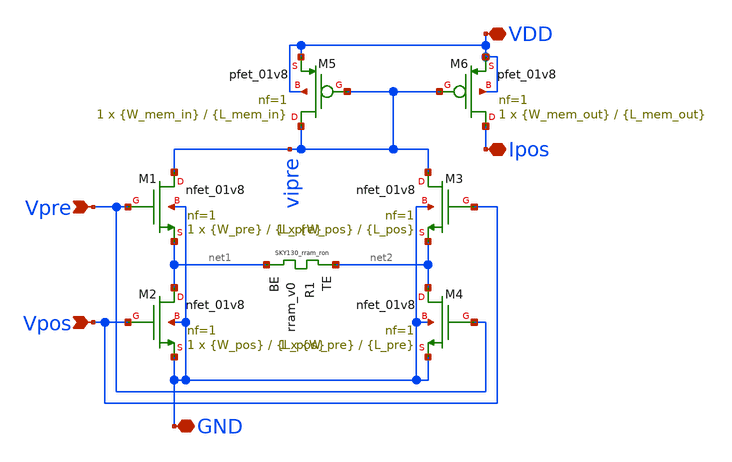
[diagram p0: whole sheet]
** sch_path: SNN/Syn_6T1R.sch
**.subckt Syn_6T1R Vpre Vpos GND Ipos VDD
*.ipin Vpre
*.ipin Vpos
*.iopin GND
*.iopin Ipos
*.iopin VDD
XM1 vipre Vpre net1 GND sky130_fd_pr__nfet_01v8 L={L_pre} W={W_pre} nf=1 ad='int((nf+1)/2) * W/nf * 0.29'
+ as='int((nf+2)/2) * W/nf * 0.29' pd='2*int((nf+1)/2) * (W/nf + 0.29)' ps='2*int((nf+2)/2) * (W/nf + 0.29)'
+ nrd='0.29 / W' nrs='0.29 / W' sa=0 sb=0 sd=0 mult=1 m=1
XR1 net2 net1 rram_v0
XM3 vipre Vpos net2 GND sky130_fd_pr__nfet_01v8 L={L_pos} W={W_pos} nf=1 ad='int((nf+1)/2) * W/nf * 0.29'
+ as='int((nf+2)/2) * W/nf * 0.29' pd='2*int((nf+1)/2) * (W/nf + 0.29)' ps='2*int((nf+2)/2) * (W/nf + 0.29)'
+ nrd='0.29 / W' nrs='0.29 / W' sa=0 sb=0 sd=0 mult=1 m=1
XM6 Ipos vipre VDD VDD sky130_fd_pr__pfet_01v8 L={L_mem_out} W={W_mem_out} nf=1 ad='int((nf+1)/2) * W/nf * 0.29'
+ as='int((nf+2)/2) * W/nf * 0.29' pd='2*int((nf+1)/2) * (W/nf + 0.29)' ps='2*int((nf+2)/2) * (W/nf + 0.29)'
+ nrd='0.29 / W' nrs='0.29 / W' sa=0 sb=0 sd=0 mult=1 m=1
XM5 vipre vipre VDD VDD sky130_fd_pr__pfet_01v8 L={L_mem_in} W={W_mem_in} nf=1 ad='int((nf+1)/2) * W/nf * 0.29'
+ as='int((nf+2)/2) * W/nf * 0.29' pd='2*int((nf+1)/2) * (W/nf + 0.29)' ps='2*int((nf+2)/2) * (W/nf + 0.29)'
+ nrd='0.29 / W' nrs='0.29 / W' sa=0 sb=0 sd=0 mult=1 m=1
XM2 net1 Vpos GND GND sky130_fd_pr__nfet_01v8 L={L_pos} W={W_pos} nf=1 ad='int((nf+1)/2) * W/nf * 0.29'
+ as='int((nf+2)/2) * W/nf * 0.29' pd='2*int((nf+1)/2) * (W/nf + 0.29)' ps='2*int((nf+2)/2) * (W/nf + 0.29)'
+ nrd='0.29 / W' nrs='0.29 / W' sa=0 sb=0 sd=0 mult=1 m=1
XM4 net2 Vpre GND GND sky130_fd_pr__nfet_01v8 L={L_pre} W={W_pre} nf=1 ad='int((nf+1)/2) * W/nf * 0.29'
+ as='int((nf+2)/2) * W/nf * 0.29' pd='2*int((nf+1)/2) * (W/nf + 0.29)' ps='2*int((nf+2)/2) * (W/nf + 0.29)'
+ nrd='0.29 / W' nrs='0.29 / W' sa=0 sb=0 sd=0 mult=1 m=1
**.ends
.end
